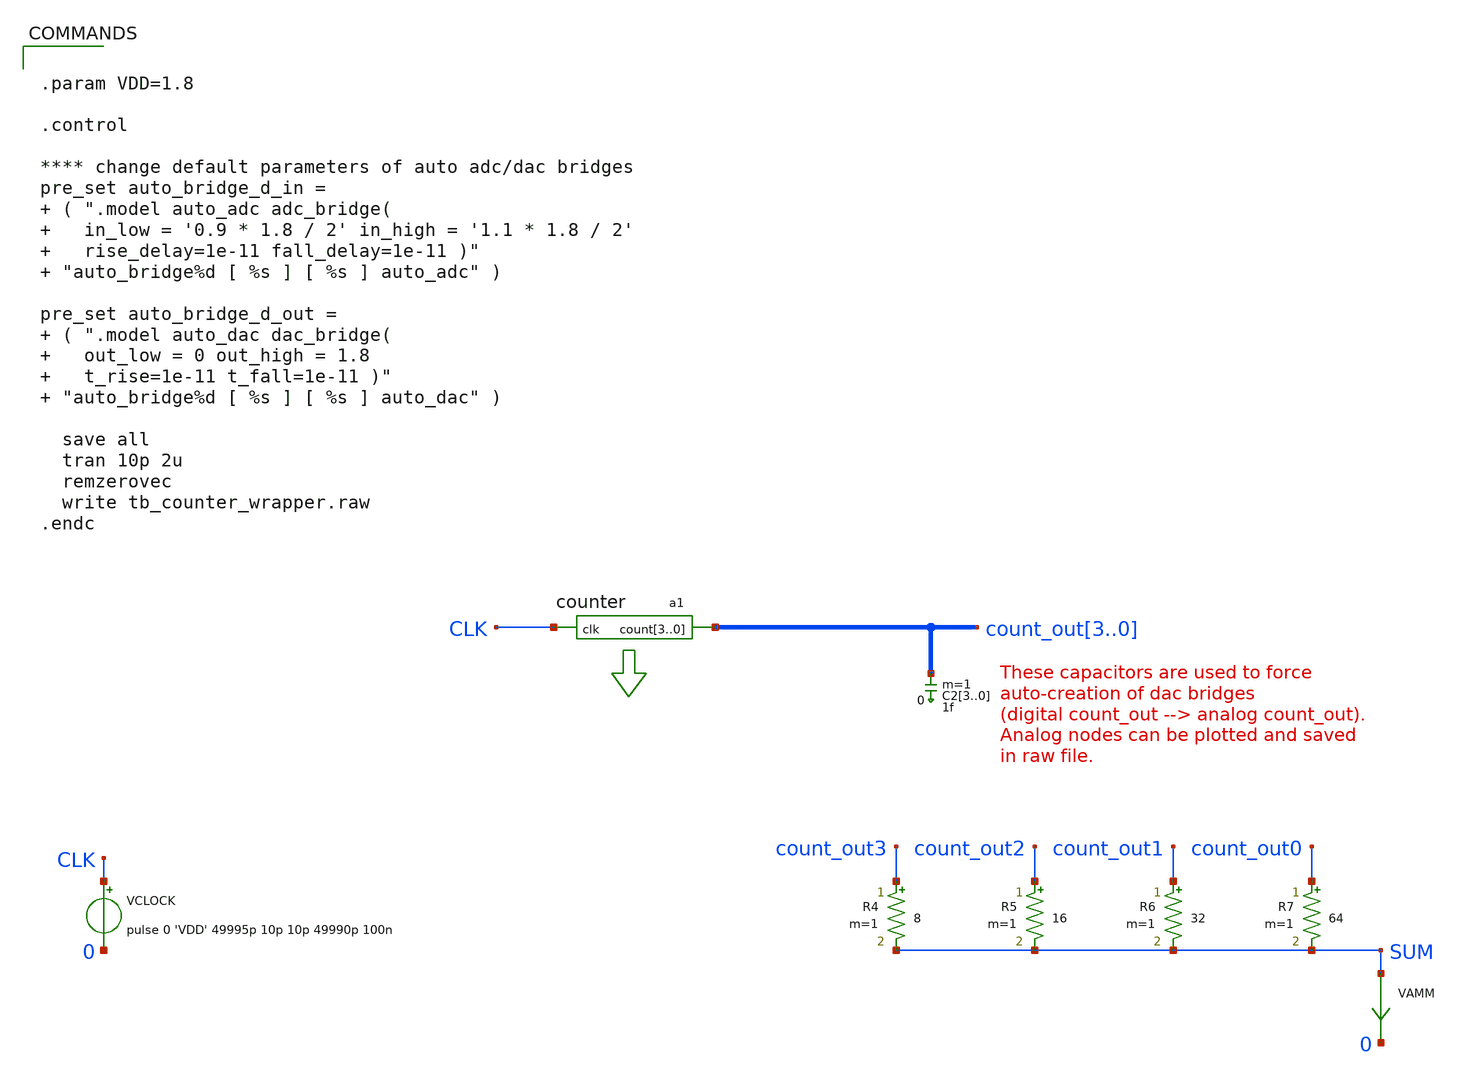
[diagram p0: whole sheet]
** sch_path: xschem_libraries_oa/ngspice_verilog_cosim/tb_counter_wrapper/schematic/tb_counter_wrapper.sch
**.subckt tb_counter_wrapper
VCLOCK CLK 0 pulse 0 'VDD' 49995p 10p 10p 49990p 100n
a1 [ CLK ] [ count_out3 count_out2 count_out1 count_out0 ] counter
C23 count_out3 0 1f m=1
C22 count_out2 0 1f m=1
C21 count_out1 0 1f m=1
C20 count_out0 0 1f m=1
VAMM SUM 0 0
R4 count_out3 SUM 8 m=1
R5 count_out2 SUM 16 m=1
R6 count_out1 SUM 32 m=1
R7 count_out0 SUM 64 m=1
**** begin user architecture code


.param VDD=1.8

.control

**** change default parameters of auto adc/dac bridges
pre_set auto_bridge_d_in =  ( ".model auto_adc adc_bridge(    in_low = '0.9 * 1.8 / 2' in_high = '1.1 * 1.8 / 2'
+    rise_delay=1e-11 fall_delay=1e-11 )"  "auto_bridge%d [ %s ] [ %s ] auto_adc" )

pre_set auto_bridge_d_out =  ( ".model auto_dac dac_bridge(    out_low = 0 out_high = 1.8
+    t_rise=1e-11 t_fall=1e-11 )"  "auto_bridge%d [ %s ] [ %s ] auto_dac" )

  save all
  tran 10p 2u
  remzerovec
  write tb_counter_wrapper.raw
.endc


**** end user architecture code
**.ends
**** begin user architecture code
.model counter d_cosim simulation="ivlng" sim_args=["counter"] delay=0
**** end user architecture code
.end
